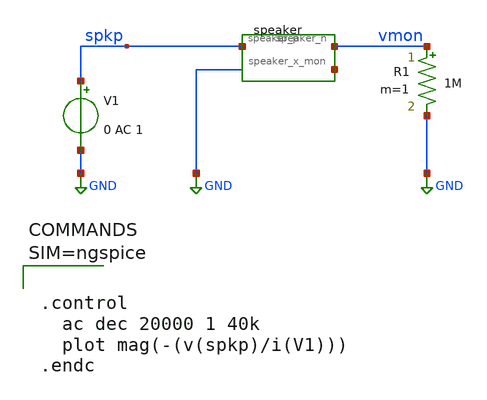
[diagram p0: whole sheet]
** sch_path: examples/analog_speaker/ac.sch
**.subckt ac
V1 spkp GND 0 AC 1
R1 vmon GND 1M m=1
Xspeaker1 spkp vmon net1 speaker
**** begin user architecture code



.control
  ac dec 20000 1 40k
  plot mag(-(v(spkp)/i(V1)))
.endc



**** end user architecture code
**.ends

* expanding   symbol:  speaker.sym # of pins=3
** sym_path: examples/analog_speaker/speaker.sym
.include /workspace/speaker.spice
.GLOBAL GND
.end
